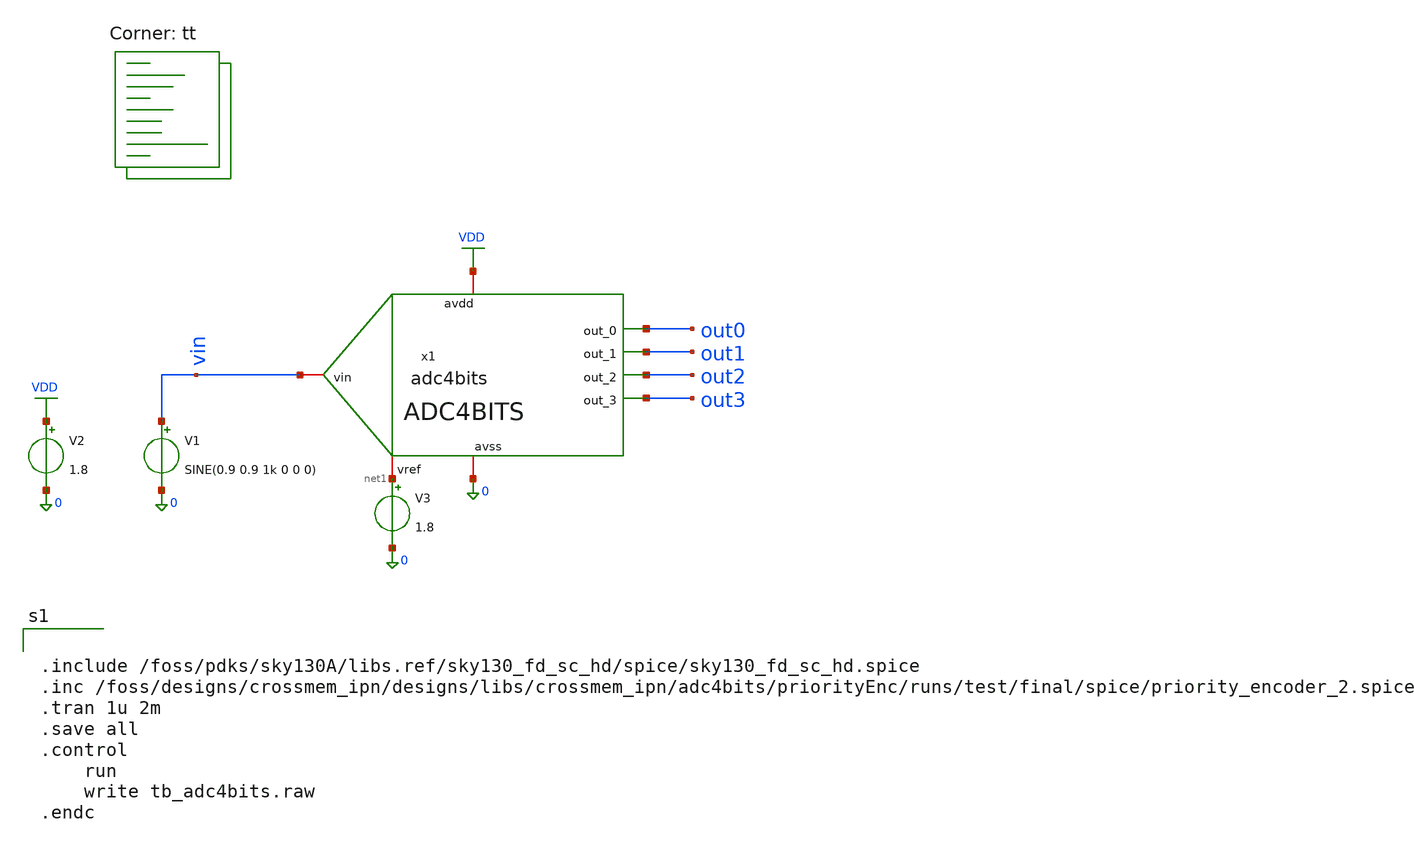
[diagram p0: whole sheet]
** sch_path: designs/libs/crossmem_ipn/adc4bits/tb_adc4bits.sch
**.subckt tb_adc4bits
V1 vin 0 SINE(0.9 0.9 1k 0 0 0)
x1 vin net1 out0 out1 out2 out3 0 VDD adc4bits
V2 VDD 0 1.8
V3 net1 0 1.8
**** begin user architecture code


.include /foss/pdks/sky130A/libs.ref/sky130_fd_sc_hd/spice/sky130_fd_sc_hd.spice
.inc /foss/designs/crossmem_ipn/designs/libs/crossmem_ipn/adc4bits/priorityEnc/runs/test/final/spice/priority_encoder_2.spice
.tran 1u 2m
.save all
.control
	run
	write tb_adc4bits.raw
.endc


.lib $::SKYWATER_MODELS/sky130.lib.spice tt
**** end user architecture code
**.ends

* expanding   symbol:  adc4bits.sym # of pins=8
** sym_path: designs/libs/crossmem_ipn/adc4bits/adc4bits.sym
** sch_path: designs/libs/crossmem_ipn/adc4bits/adc4bits.sch
.subckt adc4bits vin vref out_0 out_1 out_2 out_3 avss avdd
*.iopin vref
*.iopin avss
*.iopin vin
*.opin out_0
*.opin out_1
*.opin out_2
*.opin out_3
*.iopin avdd
x1 avdd vin vref n1 net15 avss opamp
x2 avdd vin net1 n2 net16 avss opamp
x3 avdd vin net2 n3 net17 avss opamp
x4 avdd vin net3 n4 net18 avss opamp
x5 avdd vin net4 n5 net19 avss opamp
x6 avdd vin net5 n6 net20 avss opamp
x7 avdd vin net6 n7 net21 avss opamp
x8 avdd vin net7 n8 net22 avss opamp
x9 avdd vin net8 n9 net23 avss opamp
x10 avdd vin net9 n10 net24 avss opamp
x11 avdd vin net10 n11 net25 avss opamp
x12 avdd vin net11 n12 net26 avss opamp
x13 avdd vin net12 n13 net27 avss opamp
x14 avdd vin net13 n14 net28 avss opamp
x15 avdd vin net14 n15 net29 avss opamp
x16 avss avdd n1 n11 n12 n13 n14 n15 avss n2 n3 n4 n5 n6 n7 n8 n9 n10 out_0 out_1 out_2 out_3
+ priority_encoder
R1 net1 vref sky130_fd_pr__res_generic_l1 W=1 L=3.75 m=1
R2 net2 net1 sky130_fd_pr__res_generic_l1 W=1 L=3.75 m=1
R3 net3 net2 sky130_fd_pr__res_generic_l1 W=1 L=3.75 m=1
R4 net4 net3 sky130_fd_pr__res_generic_l1 W=1 L=3.75 m=1
R5 net5 net4 sky130_fd_pr__res_generic_l1 W=1 L=3.75 m=1
R6 net6 net5 sky130_fd_pr__res_generic_l1 W=1 L=3.75 m=1
R7 net7 net6 sky130_fd_pr__res_generic_l1 W=1 L=3.75 m=1
R8 net8 net7 sky130_fd_pr__res_generic_l1 W=1 L=3.75 m=1
R9 net9 net8 sky130_fd_pr__res_generic_l1 W=1 L=3.75 m=1
R10 net10 net9 sky130_fd_pr__res_generic_l1 W=1 L=3.75 m=1
R11 net11 net10 sky130_fd_pr__res_generic_l1 W=1 L=3.75 m=1
R12 net12 net11 sky130_fd_pr__res_generic_l1 W=1 L=3.75 m=1
R13 net13 net12 sky130_fd_pr__res_generic_l1 W=1 L=3.75 m=1
R14 net14 net13 sky130_fd_pr__res_generic_l1 W=1 L=3.75 m=1
R15 avss net14 sky130_fd_pr__res_generic_l1 W=1 L=3.75 m=1
.ends


* expanding   symbol:  /foss/designs/crossmem_ipn/designs/libs/crossmem_ipn/opamp/opamp.sym # of
*+ pins=6
** sym_path: designs/libs/crossmem_ipn/opamp/opamp.sym
** sch_path: designs/libs/crossmem_ipn/opamp/opamp.sch
.subckt opamp vdd vin1 vin2 vout iref vss
*.iopin vss
*.iopin vdd
*.opin vout
*.ipin iref
*.ipin vin1
*.ipin vin2
XM3 net1 net1 vdd vdd sky130_fd_pr__pfet_01v8 L=1 W=9 nf=1 ad='int((1 + 1)/2) * 9 / 1 * 0.29' as='int((1 + 2)/2) * 9 / 1 * 0.29'
+ pd='2*int((1 + 1)/2) * (9 / 1 + 0.29)' ps='2*int((1 + 2)/2) * (9 / 1 + 0.29)' nrd='0.29 / 9 ' nrs='0.29 / 9 '
+ sa=0 sb=0 sd=0 mult=1 m=1
XM4 net2 net1 vdd vdd sky130_fd_pr__pfet_01v8 L=1 W=9 nf=1 ad='int((1 + 1)/2) * 9 / 1 * 0.29' as='int((1 + 2)/2) * 9 / 1 * 0.29'
+ pd='2*int((1 + 1)/2) * (9 / 1 + 0.29)' ps='2*int((1 + 2)/2) * (9 / 1 + 0.29)' nrd='0.29 / 9 ' nrs='0.29 / 9 '
+ sa=0 sb=0 sd=0 mult=1 m=1
XM6 vout net2 vdd vdd sky130_fd_pr__pfet_01v8 L=1 W=8.65 nf=20 ad='int((20 + 1)/2) * 8.65 / 20 * 0.29'
+ as='int((20 + 2)/2) * 8.65 / 20 * 0.29' pd='2*int((20 + 1)/2) * (8.65 / 20 + 0.29)' ps='2*int((20 + 2)/2) * (8.65 / 20 + 0.29)'
+ nrd='0.29 / 8.65 ' nrs='0.29 / 8.65 ' sa=0 sb=0 sd=0 mult=1 m=1
XM1 net1 vin1 net3 vss sky130_fd_pr__nfet_01v8 L=1 W=5 nf=1 ad='int((1 + 1)/2) * 5 / 1 * 0.29' as='int((1 + 2)/2) * 5 / 1 * 0.29'
+ pd='2*int((1 + 1)/2) * (5 / 1 + 0.29)' ps='2*int((1 + 2)/2) * (5 / 1 + 0.29)' nrd='0.29 / 5 ' nrs='0.29 / 5 '
+ sa=0 sb=0 sd=0 mult=1 m=1
XM2 net2 vin2 net3 vss sky130_fd_pr__nfet_01v8 L=1 W=5 nf=1 ad='int((1 + 1)/2) * 5 / 1 * 0.29' as='int((1 + 2)/2) * 5 / 1 * 0.29'
+ pd='2*int((1 + 1)/2) * (5 / 1 + 0.29)' ps='2*int((1 + 2)/2) * (5 / 1 + 0.29)' nrd='0.29 / 5 ' nrs='0.29 / 5 '
+ sa=0 sb=0 sd=0 mult=1 m=1
XM5 net3 iref vss vss sky130_fd_pr__nfet_01v8 L=1 W=8 nf=1 ad='int((1 + 1)/2) * 8 / 1 * 0.29' as='int((1 + 2)/2) * 8 / 1 * 0.29'
+ pd='2*int((1 + 1)/2) * (8 / 1 + 0.29)' ps='2*int((1 + 2)/2) * (8 / 1 + 0.29)' nrd='0.29 / 8 ' nrs='0.29 / 8 '
+ sa=0 sb=0 sd=0 mult=1 m=1
XM8 iref iref vss vss sky130_fd_pr__nfet_01v8 L=1 W=8 nf=1 ad='int((1 + 1)/2) * 8 / 1 * 0.29' as='int((1 + 2)/2) * 8 / 1 * 0.29'
+ pd='2*int((1 + 1)/2) * (8 / 1 + 0.29)' ps='2*int((1 + 2)/2) * (8 / 1 + 0.29)' nrd='0.29 / 8 ' nrs='0.29 / 8 '
+ sa=0 sb=0 sd=0 mult=1 m=1
XM7 vout iref vss vss sky130_fd_pr__nfet_01v8 L=1 W=7 nf=16 ad='int((16 + 1)/2) * 7 / 16 * 0.29' as='int((16 + 2)/2) * 7 / 16 * 0.29'
+ pd='2*int((16 + 1)/2) * (7 / 16 + 0.29)' ps='2*int((16 + 2)/2) * (7 / 16 + 0.29)' nrd='0.29 / 7 ' nrs='0.29 / 7 '
+ sa=0 sb=0 sd=0 mult=1 m=1
XC1 net2 vout sky130_fd_pr__cap_mim_m3_1 W=38.73 L=38.73 MF=1 m=1
.ends

.GLOBAL VDD
.end
